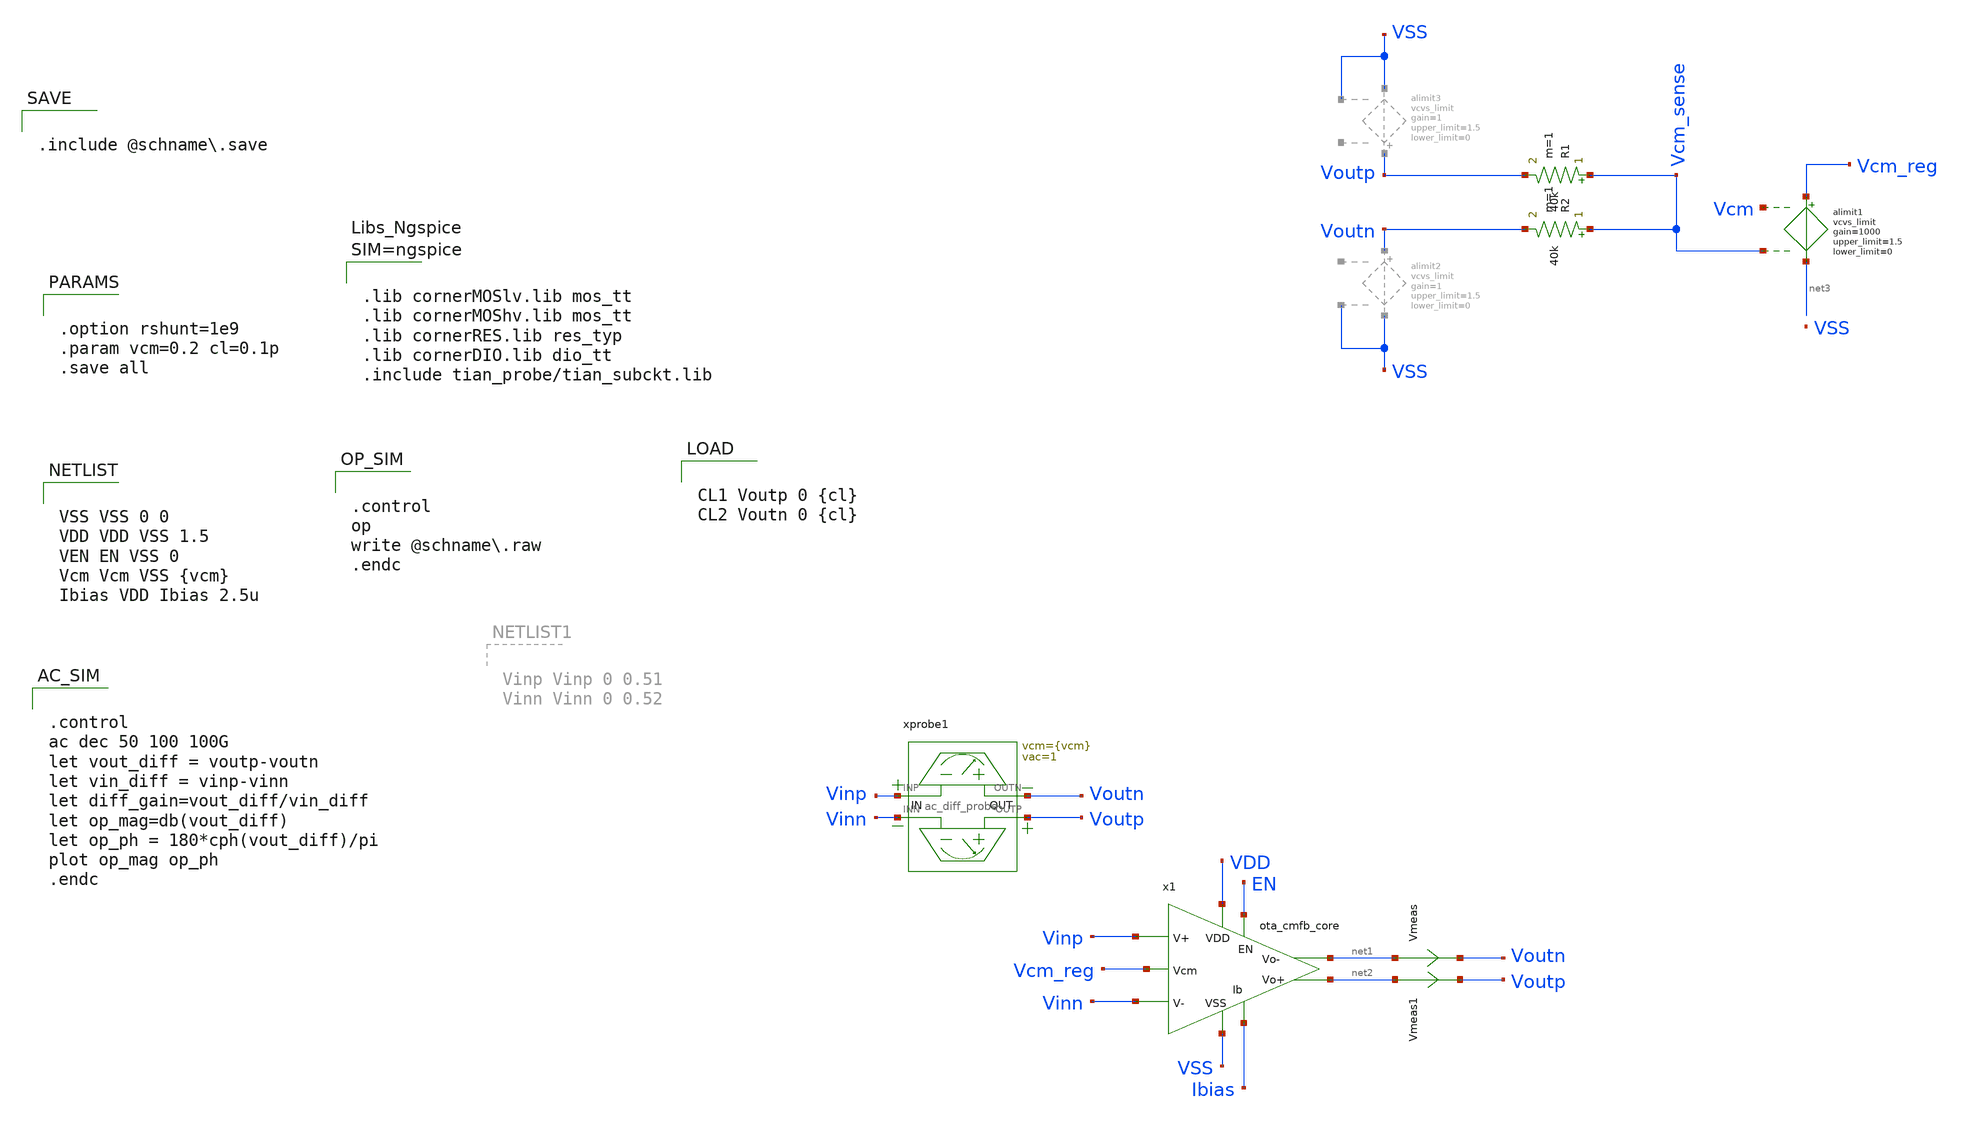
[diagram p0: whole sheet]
** sch_path: schema/ota_cmfb_core/ota_cmfb_core_tb.sch
**.subckt ota_cmfb_core_tb
x1 VDD Vcm_reg Vinn Vinp Ibias net1 net2 VSS EN ota_cmfb_core
alimit1 %vd( Vcm Vcm_sense ) %vd( Vcm_reg net3 ) alimit1
.model alimit1 limit ( gain=1000 out_lower_limit=0 out_upper_limit=1.5 )
xprobe1 Vinp Voutn Vinn Voutp ac_diff_probe vcm={vcm} vac=1
R1 Vcm_sense Voutp 40k m=1
R2 Vcm_sense Voutn 40k m=1
Vmeas net1 Voutn 0
.save i(vmeas)
Vmeas1 net2 Voutp 0
.save i(vmeas1)
**** begin user architecture code


VSS VSS 0 0
VDD VDD VSS 1.5
VEN EN VSS 0
Vcm Vcm VSS {vcm}
Ibias VDD Ibias 2.5u



.control
op
write @schname.raw
.endc




.lib cornerMOSlv.lib mos_tt
.lib cornerMOShv.lib mos_tt
.lib cornerRES.lib res_typ
.lib cornerDIO.lib dio_tt
.include tian_probe/tian_subckt.lib





.control
ac dec 50 100 100G
let vout_diff = voutp-voutn
let vin_diff = vinp-vinn
let diff_gain=vout_diff/vin_diff
let op_mag=db(vout_diff)
let op_ph = 180*cph(vout_diff)/pi
plot op_mag op_ph
.endc




.option rshunt=1e9
.param vcm=0.2 cl=0.1p
.save all




CL1 Voutp 0 {cl}
CL2 Voutn 0 {cl}



.include @schname.save

**** end user architecture code
**.ends

* expanding   symbol:  ota_cmfb_core/ota_cmfb_core.sym # of pins=9
** sym_path: schema/ota_cmfb_core/ota_cmfb_core.sym
** sch_path: schema/ota_cmfb_core/ota_cmfb_core.sch
.subckt ota_cmfb_core VDD Vcm_reg Vinn Vinp Ibias Voutn Voutp VSS EN
*.opin Voutn
*.opin Voutp
*.iopin VDD
*.iopin VSS
*.ipin Vinp
*.ipin Ibias
*.ipin Vinn
*.ipin Vcm_reg
*.ipin EN
XMD Voutp_st1 Ibias VSS VSS sg13_lv_nmos w=0.25u l=10u ng=1 m=8 mm_ok=1
XMB src_ab Vinn Voutp_st1 VDD sg13_lv_pmos w=2.5u l=2u ng=1 m=8 mm_ok=1
XMC Voutn_st1 Ibias VSS VSS sg13_lv_nmos w=0.25u l=10u ng=1 m=8 mm_ok=1
XMA src_ab Vinp Voutn_st1 VDD sg13_lv_pmos w=2.5u l=2u ng=1 m=8 mm_ok=1
XMM VDD Vcm_reg src_ab VDD sg13_lv_pmos w=2.5u l=10u ng=1 m=8 mm_ok=1
XME Ibias Ibias VSS VSS sg13_lv_nmos w=0.25u l=10u ng=1 m=2 mm_ok=1
xsf1 VDD Voutn_st1 Voutp Ibias VSS ota_cmfb_core_push_pull_output_stage
xsf2 VDD Voutp_st1 Voutn Ibias VSS ota_cmfb_core_push_pull_output_stage
XMN0 EN_N EN VSS VSS sg13_lv_nmos w=2.96u l=130.00n ng=1 m=1 mm_ok=1
XMP0 EN_N EN VDD VDD sg13_lv_pmos w=4.48u l=130.00n ng=1 m=1 mm_ok=1
XMN1 Ibias EN_N VSS VSS sg13_lv_nmos w=740.00n l=130.00n ng=1 m=1 mm_ok=1
XMB1 VDD VDD src_ab VDD sg13_lv_pmos w=2.5u l=0.5u ng=1 m=4 mm_ok=1
.ends


* expanding   symbol:  ac_diff_probe/ac_diff_probe.sym # of pins=4
** sym_path: schema/ac_diff_probe/ac_diff_probe.sym
** sch_path: schema/ac_diff_probe/ac_diff_probe.sch
.subckt ac_diff_probe INP OUTN INN OUTP  vcm=0.75 vac=0.1
*.iopin OUTN
*.iopin INP
*.iopin OUTP
*.iopin INN
xprobe1 OUTN INP ac_probe vcm={vcm} vac={vac}
xprobe2 OUTP INN ac_probe vcm={vcm} vac=-{vac}
.ends


* expanding   symbol:  ota_cmfb_core/ota_cmfb_core_push_pull_output_stage.sym # of pins=5
** sym_path: schema/ota_cmfb_core/ota_cmfb_core_push_pull_output_stage.sym
** sch_path: schema/ota_cmfb_core/ota_cmfb_core_push_pull_output_stage.sch
.subckt ota_cmfb_core_push_pull_output_stage VDD Vin Vout Vbias VSS
*.iopin VSS
*.iopin VDD
*.ipin Vbias
*.ipin Vin
*.opin Vout
XM1 Vout Vin_shifted VSS VSS sg13_lv_nmos w=0.5u l=10u ng=1 m=1 mm_ok=1
XM2 VDD Vin Vout VDD sg13_lv_pmos w=5u l=0.5u ng=1 m=1 mm_ok=1
XMC VDD Vbiasp CD_DRN VDD sg13_lv_pmos w=2.5u l=3u ng=1 m=4 mm_ok=1
XME Vin_shifted Vcasp2 Vin VDD sg13_lv_pmos w=2.5u l=3u ng=1 m=2 mm_ok=1
XMD CD_DRN Vcasp Vin VDD sg13_lv_pmos w=2.5u l=3u ng=1 m=4 mm_ok=1
XMN Vin Vcasn2 Vin_shifted VSS sg13_lv_nmos w=0.7u l=3u ng=1 m=2 mm_ok=1
XMH VDD Vbiasp net1 VDD sg13_lv_pmos w=2.5u l=3u ng=1 m=4 mm_ok=1
XMI net1 Vcasp Vcasp VDD sg13_lv_pmos w=2.5u l=3u ng=1 m=4 mm_ok=1
XMJ Vcasp Vcasp2 Vcasp2 VDD sg13_lv_pmos w=2.5u l=3u ng=1 m=4 mm_ok=1
XMB VDD Vbiasp Vcasn2 VDD sg13_lv_pmos w=2.5u l=3u ng=1 m=4 mm_ok=1
XMO Vcasn2 Vcasn2 Vcasn VSS sg13_lv_nmos w=0.7u l=3u ng=1 m=4 mm_ok=1
XR1 net2 Vout VSS rhigh w=0.5e-6 l=1e-6*8 m=1 b=0 mm_ok=1
XC1 Vin net2 sg13_moscap_p w=3.5u l=21.5u m=1 mm_ok=1
XMFG Vbiasp Vbias VSS VSS sg13_lv_nmos w=0.25u l=10u ng=1 m=2 mm_ok=1
XMA VDD Vbiasp Vbiasp VDD sg13_lv_pmos w=2.5u l=3u ng=1 m=10 mm_ok=1
XMP Vcasn Vcasn Vbiasn VSS sg13_lv_nmos w=0.7u l=3u ng=1 m=4 mm_ok=1
XMQ Vbiasn Vbiasn VSS VSS sg13_lv_nmos w=0.7u l=3u ng=1 m=4 mm_ok=1
XMM Vin_shifted Vcasn src_ml VSS sg13_lv_nmos w=0.7u l=3u ng=1 m=4 mm_ok=1
XML src_ml Vbiasn VSS VSS sg13_lv_nmos w=0.7u l=3u ng=1 m=4 mm_ok=1
XMK Vcasp2 Vbiasn VSS VSS sg13_lv_nmos w=0.7u l=3u ng=1 m=4 mm_ok=1
XM3 CD_DRN VDD VDD VDD sg13_lv_pmos w=2.5u l=0.5u ng=1 m=2 mm_ok=1
XM4 Vin_shifted VDD VDD VDD sg13_lv_pmos w=2.5u l=0.5u ng=1 m=1 mm_ok=1
XM5 Vbiasp VDD VDD VDD sg13_lv_pmos w=2.5u l=0.5u ng=1 m=1 mm_ok=1
XM6 Vin VDD VDD VDD sg13_lv_pmos w=2.5u l=0.5u ng=1 m=1 mm_ok=1
XM7 VSS VSS Vin_shifted VSS sg13_lv_nmos w=0.7u l=0.5u ng=1 m=2 mm_ok=1
XM8 VSS VSS Vcasn VSS sg13_lv_nmos w=0.7u l=0.5u ng=1 m=4 mm_ok=1
XMX VSS VSS Vin_shifted VSS sg13_lv_nmos w=0.7u l=3u ng=1 m=4 mm_ok=1
XM9 VSS VSS src_ml VSS sg13_lv_nmos w=0.7u l=0.5u ng=1 m=4 mm_ok=1
XM10 Vcasp VDD VDD VDD sg13_lv_pmos w=2.5u l=0.5u ng=1 m=2 mm_ok=1
XM12 VSS VSS Vbiasp VSS sg13_lv_nmos w=0.25u l=0.5u ng=1 m=2 mm_ok=1
.ends


* expanding   symbol:  ac_probe/ac_probe.sym # of pins=2
** sym_path: schema/ac_probe/ac_probe.sym
** sch_path: schema/ac_probe/ac_probe.sch
.subckt ac_probe OUT IN  vcm=0.75 vac=0.01

*.iopin IN
*.iopin OUT
C1 0 IN 1 m=1
V1 IN 0 {vcm} ac {vac}
R1 OUT IN 1G m=1
.ends

.end
